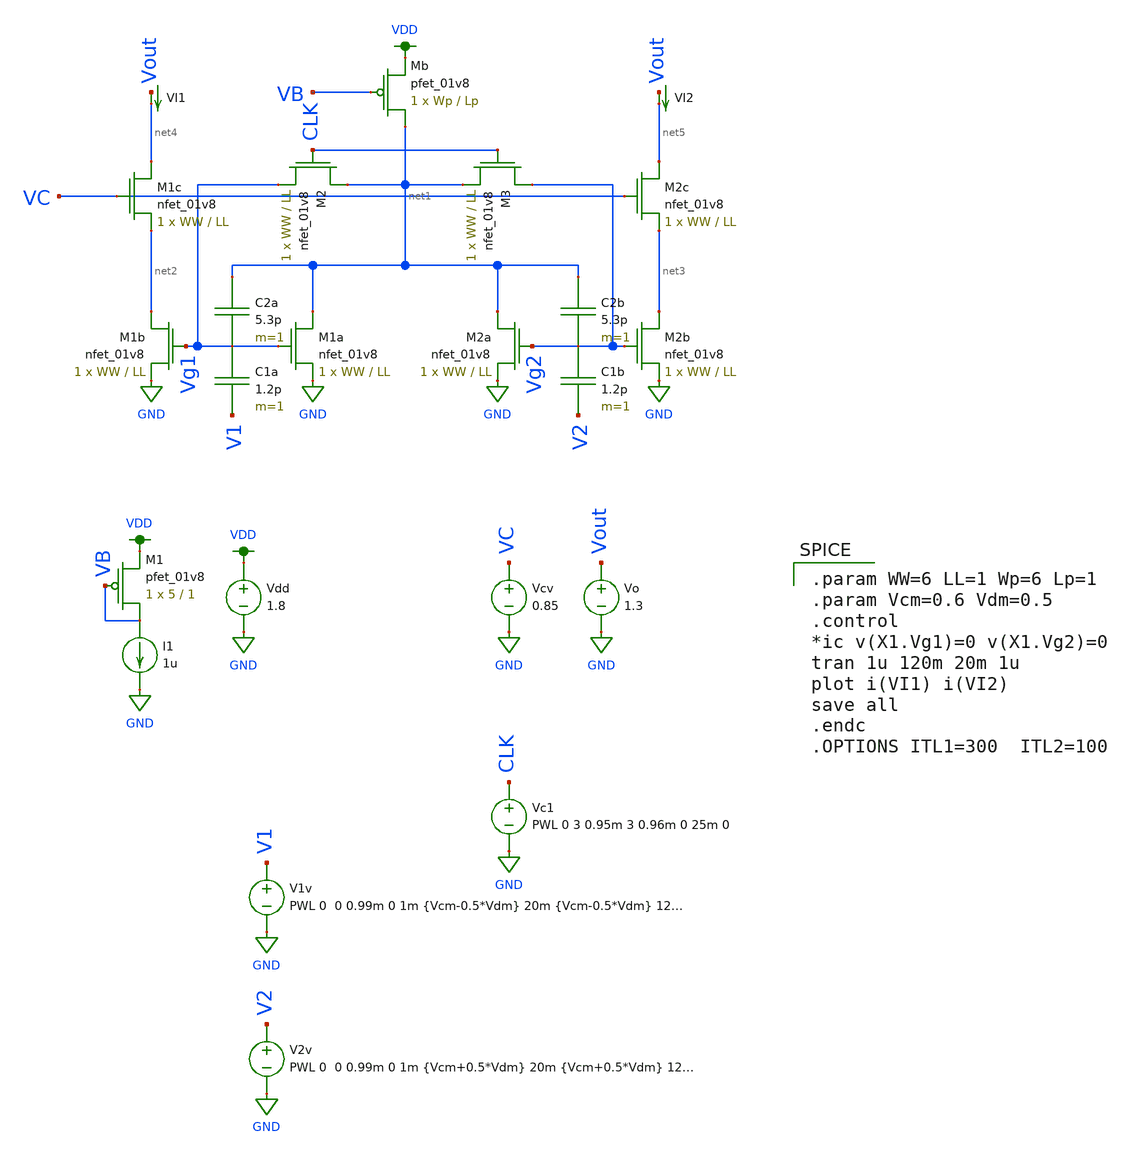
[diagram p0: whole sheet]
** sch_path: schematic/test/fgmos_diffpair_test.sch
**.subckt fgmos_diffpair_test
VI1 Vout net4 0
.save i(vi1)
VI2 Vout net5 0
.save i(vi2)
V1v V1 GND PWL 0 0 0.99m 0 1m {Vcm-0.5*Vdm} 20m {Vcm-0.5*Vdm} 120m {Vcm+0.5*Vdm}
V2v V2 GND PWL 0 0 0.99m 0 1m {Vcm+0.5*Vdm} 20m {Vcm+0.5*Vdm} 120m {Vcm-0.5*Vdm}
Vdd VDD GND 1.8
Vcv VC GND 0.85
XM1 VB VB VDD VDD sky130_fd_pr__pfet_01v8 L=1 W=5 nf=1 ad='int((nf+1)/2) * W/nf * 0.29' as='int((nf+2)/2) * W/nf * 0.29'
+ pd='2*int((nf+1)/2) * (W/nf + 0.29)' ps='2*int((nf+2)/2) * (W/nf + 0.29)' nrd='0.29 / W' nrs='0.29 / W'
+ sa=0 sb=0 sd=0 mult=1 m=1
I1 VB GND 1u
XM1a net1 Vg1 GND GND sky130_fd_pr__nfet_01v8 L=LL W=WW nf=1 ad='int((nf+1)/2) * W/nf * 0.29' as='int((nf+2)/2) * W/nf * 0.29'
+ pd='2*int((nf+1)/2) * (W/nf + 0.29)' ps='2*int((nf+2)/2) * (W/nf + 0.29)' nrd='0.29 / W' nrs='0.29 / W'
+ sa=0 sb=0 sd=0 mult=1 m=1
XM1b net2 Vg1 GND GND sky130_fd_pr__nfet_01v8 L=LL W=WW nf=1 ad='int((nf+1)/2) * W/nf * 0.29' as='int((nf+2)/2) * W/nf * 0.29'
+ pd='2*int((nf+1)/2) * (W/nf + 0.29)' ps='2*int((nf+2)/2) * (W/nf + 0.29)' nrd='0.29 / W' nrs='0.29 / W'
+ sa=0 sb=0 sd=0 mult=1 m=1
XM1c net4 VC net2 GND sky130_fd_pr__nfet_01v8 L=LL W=WW nf=1 ad='int((nf+1)/2) * W/nf * 0.29' as='int((nf+2)/2) * W/nf * 0.29'
+ pd='2*int((nf+1)/2) * (W/nf + 0.29)' ps='2*int((nf+2)/2) * (W/nf + 0.29)' nrd='0.29 / W' nrs='0.29 / W'
+ sa=0 sb=0 sd=0 mult=1 m=1
XM2b net3 Vg2 GND GND sky130_fd_pr__nfet_01v8 L=LL W=WW nf=1 ad='int((nf+1)/2) * W/nf * 0.29' as='int((nf+2)/2) * W/nf * 0.29'
+ pd='2*int((nf+1)/2) * (W/nf + 0.29)' ps='2*int((nf+2)/2) * (W/nf + 0.29)' nrd='0.29 / W' nrs='0.29 / W'
+ sa=0 sb=0 sd=0 mult=1 m=1
XM2a net1 Vg2 GND GND sky130_fd_pr__nfet_01v8 L=LL W=WW nf=1 ad='int((nf+1)/2) * W/nf * 0.29' as='int((nf+2)/2) * W/nf * 0.29'
+ pd='2*int((nf+1)/2) * (W/nf + 0.29)' ps='2*int((nf+2)/2) * (W/nf + 0.29)' nrd='0.29 / W' nrs='0.29 / W'
+ sa=0 sb=0 sd=0 mult=1 m=1
XM2c net5 VC net3 GND sky130_fd_pr__nfet_01v8 L=LL W=WW nf=1 ad='int((nf+1)/2) * W/nf * 0.29' as='int((nf+2)/2) * W/nf * 0.29'
+ pd='2*int((nf+1)/2) * (W/nf + 0.29)' ps='2*int((nf+2)/2) * (W/nf + 0.29)' nrd='0.29 / W' nrs='0.29 / W'
+ sa=0 sb=0 sd=0 mult=1 m=1
XMb net1 VB VDD VDD sky130_fd_pr__pfet_01v8 L=Lp W=Wp nf=1 ad='int((nf+1)/2) * W/nf * 0.29' as='int((nf+2)/2) * W/nf * 0.29'
+ pd='2*int((nf+1)/2) * (W/nf + 0.29)' ps='2*int((nf+2)/2) * (W/nf + 0.29)' nrd='0.29 / W' nrs='0.29 / W'
+ sa=0 sb=0 sd=0 mult=1 m=1
C2b net1 Vg2 5.3p m=1
C1a Vg1 V1 1.2p m=1
C1b Vg2 V2 1.2p m=1
C2a net1 Vg1 5.3p m=1
Vo Vout GND 1.3
Vc1 CLK GND PWL 0 3 0.95m 3 0.96m 0 25m 0
XM2 net1 CLK Vg1 GND sky130_fd_pr__nfet_01v8 L=LL W=WW nf=1 ad='int((nf+1)/2) * W/nf * 0.29' as='int((nf+2)/2) * W/nf * 0.29'
+ pd='2*int((nf+1)/2) * (W/nf + 0.29)' ps='2*int((nf+2)/2) * (W/nf + 0.29)' nrd='0.29 / W' nrs='0.29 / W'
+ sa=0 sb=0 sd=0 mult=1 m=1
XM3 Vg2 CLK net1 GND sky130_fd_pr__nfet_01v8 L=LL W=WW nf=1 ad='int((nf+1)/2) * W/nf * 0.29' as='int((nf+2)/2) * W/nf * 0.29'
+ pd='2*int((nf+1)/2) * (W/nf + 0.29)' ps='2*int((nf+2)/2) * (W/nf + 0.29)' nrd='0.29 / W' nrs='0.29 / W'
+ sa=0 sb=0 sd=0 mult=1 m=1
**** begin user architecture code

.option wnflag=1
.param MC_SWITCH=0.0
.lib ~/skywater/skywater-pdk/libraries/sky130_fd_pr_ngspice/latest/models/sky130.lib.spice tt


.param WW=6 LL=1 Wp=6 Lp=1
.param Vcm=0.6 Vdm=0.5
.control
*ic v(X1.Vg1)=0 v(X1.Vg2)=0
tran 1u 120m 20m 1u
plot i(VI1) i(VI2)
save all
.endc
.OPTIONS ITL1=300  ITL2=100

**** end user architecture code
**.ends
.GLOBAL GND
.GLOBAL VDD
.end
